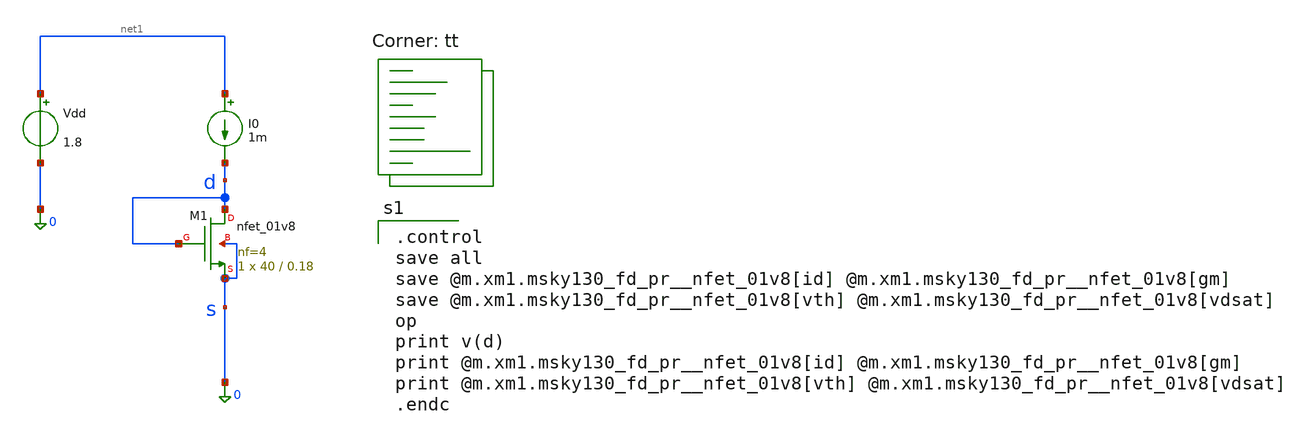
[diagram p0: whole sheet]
** sch_path: Homework 6 - Simulation on Open Source Softwares/Simulations/ex3_diode.sch
**.subckt ex3_diode
XM1 d d 0 0 sky130_fd_pr__nfet_01v8 L=0.18 W=40 nf=4 ad='int((4 + 1)/2) * 40 / 4 * 0.29' as='int((4 + 2)/2) * 40 / 4 * 0.29'
+ pd='2*int((4 + 1)/2) * (40 / 4 + 0.29)' ps='2*int((4 + 2)/2) * (40 / 4 + 0.29)' nrd='0.29 / 40 ' nrs='0.29 / 40 '
+ sa=0 sb=0 sd=0 mult=1 m=1
Vdd net1 0 1.8
I0 net1 d 1m
**** begin user architecture code
.lib $::SKYWATER_MODELS/sky130.lib.spice tt

.control
save all
save @m.xm1.msky130_fd_pr__nfet_01v8[id] @m.xm1.msky130_fd_pr__nfet_01v8[gm]
save @m.xm1.msky130_fd_pr__nfet_01v8[vth] @m.xm1.msky130_fd_pr__nfet_01v8[vdsat]
op
print v(d)
print @m.xm1.msky130_fd_pr__nfet_01v8[id] @m.xm1.msky130_fd_pr__nfet_01v8[gm]
print @m.xm1.msky130_fd_pr__nfet_01v8[vth] @m.xm1.msky130_fd_pr__nfet_01v8[vdsat]
.endc

**** end user architecture code
**.ends
.end
